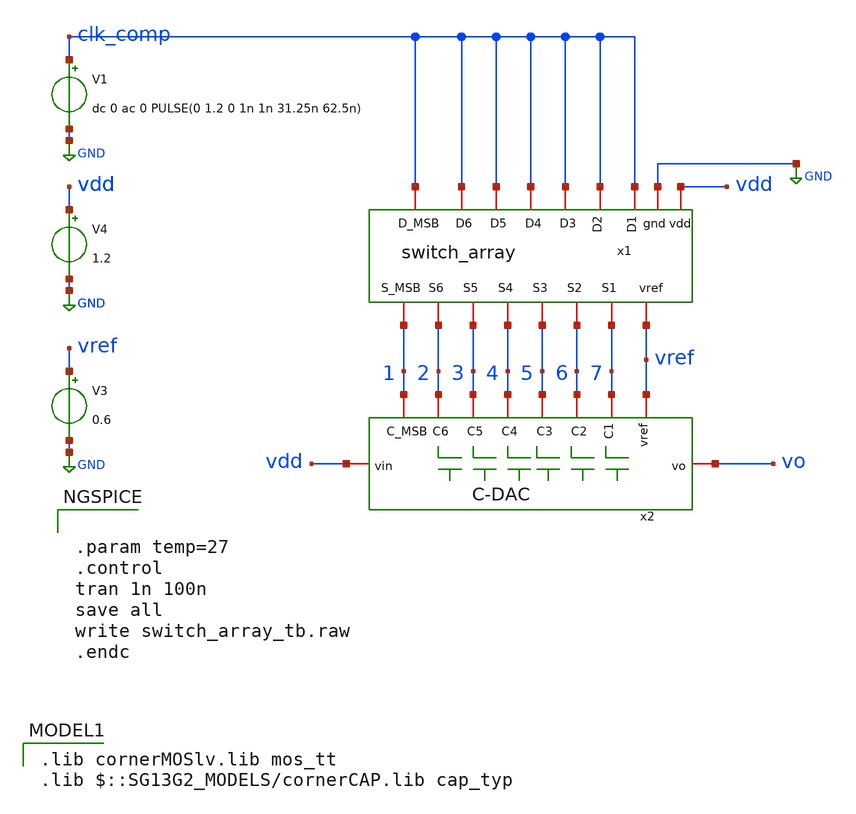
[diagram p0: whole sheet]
** sch_path: modules/module_3_8_bit_SAR_ADC/part_3_array_components/switch_array/switch_array_tb.sch
**.subckt switch_array_tb
V1 clk_comp GND dc 0 ac 0 PULSE(0 1.2 0 1n 1n 31.25n 62.5n)
V3 vref GND 0.6
V4 vdd GND 1.2
x1 vref vdd GND 3 2 clk_comp clk_comp 1 clk_comp 7 6 clk_comp clk_comp 5 clk_comp 4 clk_comp
+ switch_array
x2 vdd vo 3 2 5 4 6 7 vref 1 C-DAC
**** begin user architecture code


.param temp=27
.control
tran 1n 100n
save all
write switch_array_tb.raw
.endc


 .lib cornerMOSlv.lib mos_tt
.lib $::SG13G2_MODELS/cornerCAP.lib cap_typ

**** end user architecture code
**.ends

* expanding   symbol:  switch_array.sym # of pins=17
** sym_path: modules/module_3_8_bit_SAR_ADC/part_3_array_components/switch_array/switch_array.sym
** sch_path: modules/module_3_8_bit_SAR_ADC/part_3_array_components/switch_array/switch_array.sch
.subckt switch_array vref vdd gnd S5 S6 D5 D6 S_MSB D_MSB S1 S2 D1 D2 S3 D3 S4 D4
*.iopin S_MSB
*.iopin S6
*.iopin D_MSB
*.iopin D6
*.iopin S5
*.iopin D5
*.iopin S4
*.iopin S3
*.iopin S2
*.iopin D4
*.iopin D3
*.iopin D2
*.iopin S1
*.iopin D1
*.iopin vdd
*.iopin vref
*.iopin gnd
x1 D_MSB vref S_MSB gnd net1 vdd T_gate
x2 D4 vref S4 gnd net4 vdd T_gate
x4 net4 gnd S4 gnd D4 vdd T_gate
x5 net5 gnd S3 gnd D3 vdd T_gate
x6 net6 gnd S2 gnd D2 vdd T_gate
x8 net7 gnd S1 gnd D1 vdd T_gate
x9 D1 vref S1 gnd net7 vdd T_gate
x11 D2 vref S2 gnd net6 vdd T_gate
x12 net3 gnd S5 gnd D5 vdd T_gate
x14 D5 vref S5 gnd net3 vdd T_gate
x15 D6 vref S6 gnd net2 vdd T_gate
x17 net2 gnd S6 gnd D6 vdd T_gate
x18 net1 gnd S_MSB gnd D_MSB vdd T_gate
x20 D3 vref S3 gnd net5 vdd T_gate
x3 vdd D4 net4 gnd inverter
x7 vdd D_MSB net1 gnd inverter
x10 vdd D6 net2 gnd inverter
x13 vdd D5 net3 gnd inverter
x16 vdd D3 net5 gnd inverter
x19 vdd D2 net6 gnd inverter
x21 vdd D1 net7 gnd inverter
.ends


* expanding   symbol:  C-DAC.sym # of pins=10
** sym_path: modules/module_3_8_bit_SAR_ADC/part_3_array_components/C-DAC/C-DAC.sym
** sch_path: modules/module_3_8_bit_SAR_ADC/part_3_array_components/C-DAC/C-DAC.sch
.subckt C-DAC vin vo C5 C6 C3 C4 C2 C1 vref C_MSB
*.iopin vin
*.iopin vo
*.iopin C6
*.iopin C5
*.iopin C4
*.iopin C3
*.iopin C2
*.iopin C1
*.iopin vref
*.iopin C_MSB
XC1 vo vref cap_cmim w=5.71e-6 l=5.71e-6 m=1 mm_ok=1
XC2 vo C1 cap_cmim w=5.71e-6 l=5.71e-6 m=1 mm_ok=1
XC3 vo C2 cap_cmim w=5.71e-6 l=5.71e-6 m=2 mm_ok=1
XC4 vo C3 cap_cmim w=5.71e-6 l=5.71e-6 m=4 mm_ok=1
XC5 vo C4 cap_cmim w=5.71e-6 l=5.71e-6 m=8 mm_ok=1
XC6 vo C5 cap_cmim w=5.71e-6 l=5.71e-6 m=16 mm_ok=1
XC7 vo C6 cap_cmim w=5.71e-6 l=5.71e-6 m=32 mm_ok=1
XC8 vo C_MSB cap_cmim w=5.71e-6 l=5.71e-6 m=64 mm_ok=1
R1 vin vo 1 m=1
.ends


* expanding   symbol:  T_gate.sym # of pins=6
** sym_path: modules/module_3_8_bit_SAR_ADC/part_2_digital_comps/T_gate/schematic/T_gate.sym
** sch_path: modules/module_3_8_bit_SAR_ADC/part_2_digital_comps/T_gate/schematic/T_gate.sch
.subckt T_gate !Control Vin Vout gnd Control vdd
*.iopin Vout
*.iopin Vin
*.iopin !Control
*.iopin Control
*.iopin gnd
*.iopin vdd
XM1 Vin Control Vout gnd sg13_lv_nmos w=1u l=0.13u ng=1 m=1 mm_ok=1
XM2 Vin !Control Vout vdd sg13_lv_pmos w=2u l=0.13u ng=1 m=1 mm_ok=1
.ends


* expanding   symbol:  inverter.sym # of pins=4
** sym_path: modules/module_3_8_bit_SAR_ADC/part_2_digital_comps/bootstrap_switch/schematic/inverter.sym
** sch_path: modules/module_3_8_bit_SAR_ADC/part_2_digital_comps/bootstrap_switch/schematic/inverter.sch
.subckt inverter vdd vi vo gnd
*.iopin vi
*.iopin vo
*.iopin gnd
*.iopin vdd
XM5 vo vi vdd vdd sg13_lv_pmos w=800n l=130n ng=1 m=1 mm_ok=1
XM7 vo vi gnd gnd sg13_lv_nmos w=400n l=130n ng=1 m=1 mm_ok=1
.ends

.GLOBAL GND
.end
